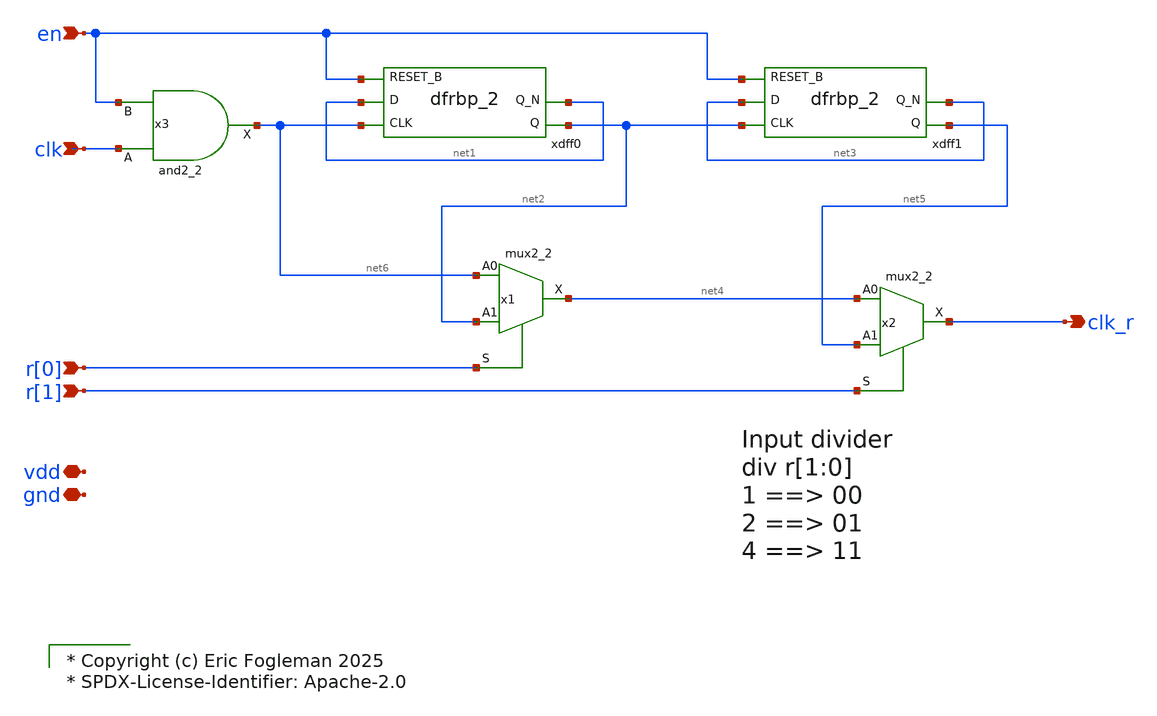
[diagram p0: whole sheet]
** sch_path: xschem/ejf_pll96_div_r.sch

* Copyright (c) Eric Fogleman 2025
* SPDX-License-Identifier: Apache-2.0

**.subckt ejf_pll96_div_r clk vdd gnd en r[0] r[1] clk_r
*.ipin clk
*.iopin vdd
*.iopin gnd
*.ipin en
*.ipin r[0]
*.ipin r[1]
*.opin clk_r
xdff0 net6 net1 en gnd gnd vdd vdd net2 net1 sky130_fd_sc_ls__dfrbp_2
x1 net6 net2 r[0] gnd gnd vdd vdd net4 sky130_fd_sc_ls__mux2_2
x2 net4 net5 r[1] gnd gnd vdd vdd clk_r sky130_fd_sc_ls__mux2_2
xdff1 net2 net3 en gnd gnd vdd vdd net5 net3 sky130_fd_sc_ls__dfrbp_2
x3 clk en gnd gnd vdd vdd net6 sky130_fd_sc_ls__and2_2
**.ends
.end
